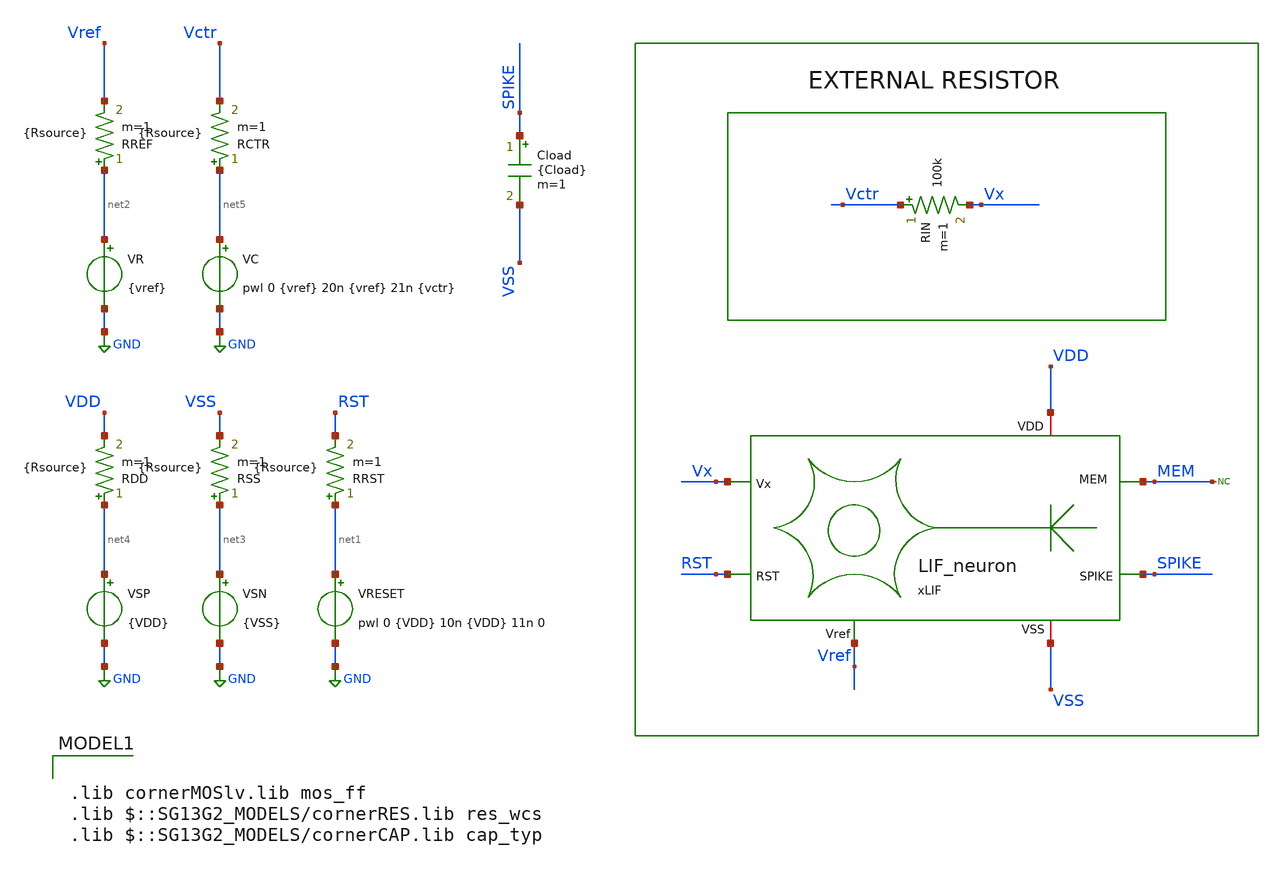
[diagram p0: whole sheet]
** sch_path: work/LIF_neuron/xschem/sweep_LIF_Neuron.sch
**.subckt sweep_LIF_Neuron
VRESET net1 GND pwl 0 {VDD} 10n {VDD} 11n 0
VSN net3 GND {VSS}
VR net2 GND {vref}
VC net5 GND pwl 0 {vref} 20n {vref} 21n {vctr}
xLIF VDD Vx MEM RST SPIKE VSS Vref LIF_neuron
RDD net4 VDD {Rsource} m=1
RSS net3 VSS {Rsource} m=1
RRST net1 RST {Rsource} m=1
RREF net2 Vref {Rsource} m=1
RCTR net5 Vctr {Rsource} m=1
Cload SPIKE VSS {Cload} m=1
RIN Vctr Vx 100k m=1
VSP net4 GND {VDD}
* noconn MEM
**** begin user architecture code



.param VDD = 1.2
.param VSS = 0
.param vctr = 1
.param vref = 0
.param Cload = 0.1p
.param Rsource = 10


.param sw_stat_global = 0
.param sw_stat_mismatch = 0

.save all

.control

* >> Variables <<
let Vhigh = 0.8
let Vmid = Vhigh * 0.5

let tstop = 50n
let tstep = tstop/1k


* Run transient analysis


=====================barrido===================

let VDD_start = 0.4
let VDD_end   = 0.6
let VDD_step  = 0.008
let idx = 0

let npoints = (VDD_end - VDD_start)/VDD_step
====================vectores===================

let VDD_vec = vector(npoints)
let spike_vec = vector(npoints)

settype voltage VDD_vec
settype voltage spike_vec

===============================================

let v = VDD_start

while v le VDD_end

  alterparam VDD = $&v

  reset
  tran 0.05n 50n

  meas tran SPIKE_max max v(SPIKE)

  let spike_vec[idx] = SPIKE_max
  let VDD_vec[idx] = v

  let v = v + VDD_step
  let idx = idx + 1

end

print v(spike_vec) v(VDD_vec)
plot spike_vec vs VDD_vec


.endc



.lib cornerMOSlv.lib mos_ff
.lib $::SG13G2_MODELS/cornerRES.lib res_wcs
.lib $::SG13G2_MODELS/cornerCAP.lib cap_typ

**** end user architecture code
**.ends
.GLOBAL GND
.end
